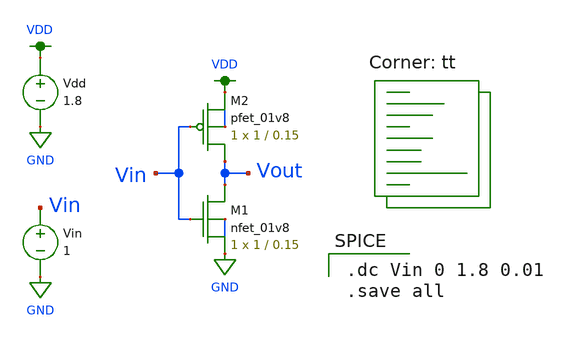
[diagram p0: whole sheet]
** sch_path: and/schematic/inverter_vtc.sch
**.subckt inverter_vtc
XM1 Vout Vin GND GND sky130_fd_pr__nfet_01v8 L=0.15 W=1 nf=1 ad='int((nf+1)/2) * W/nf * 0.29' as='int((nf+2)/2) * W/nf * 0.29'
+ pd='2*int((nf+1)/2) * (W/nf + 0.29)' ps='2*int((nf+2)/2) * (W/nf + 0.29)' nrd='0.29 / W' nrs='0.29 / W'
+ sa=0 sb=0 sd=0 mult=1 m=1
XM2 Vout Vin VDD VDD sky130_fd_pr__pfet_01v8 L=0.15 W=1 nf=1 ad='int((nf+1)/2) * W/nf * 0.29' as='int((nf+2)/2) * W/nf * 0.29'
+ pd='2*int((nf+1)/2) * (W/nf + 0.29)' ps='2*int((nf+2)/2) * (W/nf + 0.29)' nrd='0.29 / W' nrs='0.29 / W'
+ sa=0 sb=0 sd=0 mult=1 m=1
Vdd VDD GND 1.8
Vin Vin GND 1
**** begin user architecture code

.dc Vin 0 1.8 0.01
.save all

.lib $::SKYWATER_MODELS/sky130.lib.spice tt
**** end user architecture code
**.ends
.GLOBAL GND
.GLOBAL VDD
.end
